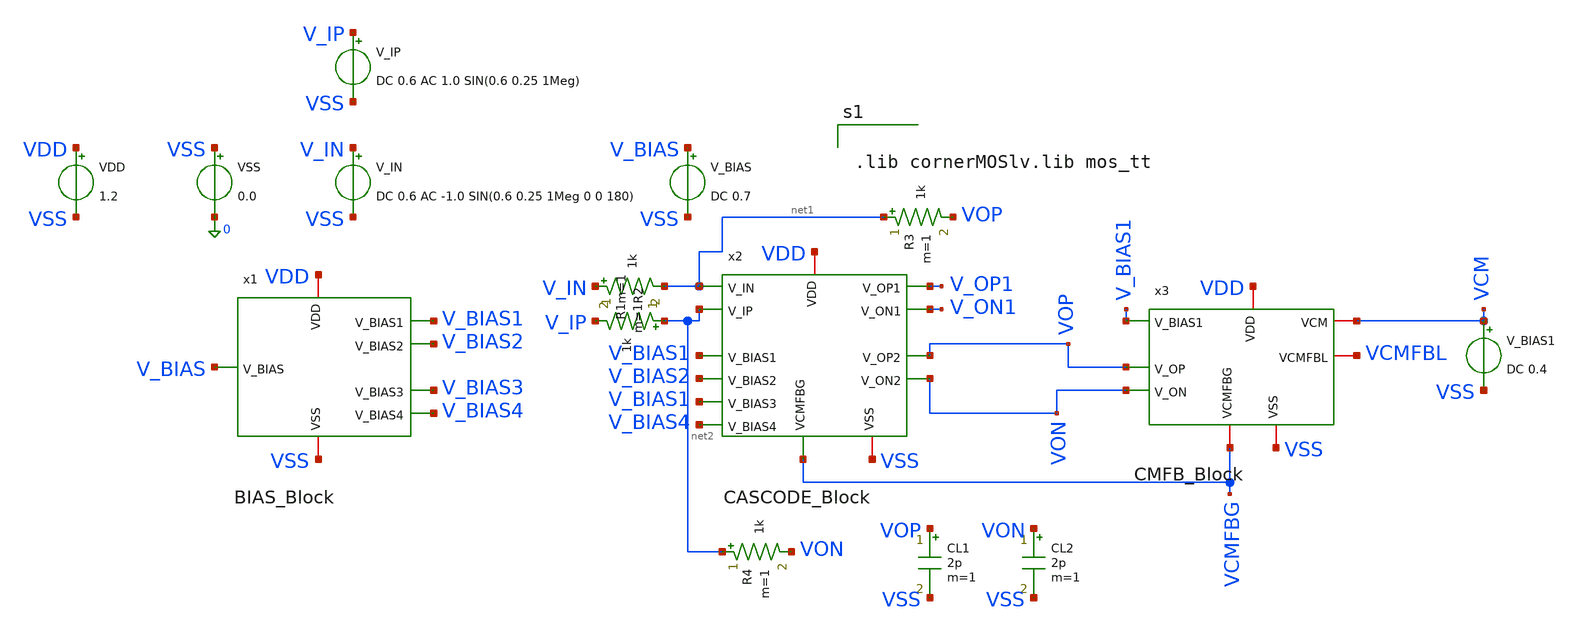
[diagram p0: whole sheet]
** sch_path: two-stage-ota-with-cmfb/Simulation/TEST_SIN.sch
**.subckt TEST_SIN
VDD VDD VSS 1.2
VSS VSS 0 0.0
V_IN V_IN VSS DC 0.6 AC -1.0 SIN(0.6 0.25 1Meg 0 0 180)
V_IP V_IP VSS DC 0.6 AC 1.0 SIN(0.6 0.25 1Meg)
V_BIAS V_BIAS VSS DC 0.7
V_BIAS1 VCM VSS DC 0.4
CL1 VOP VSS 2p m=1
x1 VSS V_BIAS4 V_BIAS2 V_BIAS3 VDD V_BIAS1 V_BIAS BIAS_Block
x2 VDD V_BIAS1 net1 net2 V_BIAS2 V_ON1 V_OP1 V_BIAS1 VON VOP VCMFBG V_BIAS4 VSS CASCODE_Block
x3 VDD V_BIAS1 VCM VOP VON VCMFBL VCMFBG VSS CMFB_Block
CL2 VON VSS 2p m=1
R1 V_IN net1 1k m=1
R2 net2 V_IP 1k m=1
R3 net1 VOP 1k m=1
R4 net2 VON 1k m=1
**** begin user architecture code


.lib cornerMOSlv.lib mos_tt




* RUN SINE RESPONSE & THD
.control
set color0=white
set color1=black

tran 1n 6u

let v_out_sine = v(vop) - v(von)
let v_in_sine  = v(v_ip) - v(v_in)

* Do bien do dinh - dinh tren cac chu ky xac lap (tu 3us den 6us)
meas tran v_max_sine max v_out_sine from=3u to=6u
meas tran v_min_sine min v_out_sine from=3u to=6u
let v_swing_pp = v_max_sine - v_min_sine

* Phan tich pho Fourier va THD
fourier 1Meg v_out_sine

echo '=========================================================================='
echo 'KET QUA LARGE-SIGNAL SINE (1 MHz):'
echo '=========================================================================='
print v_swing_pp

* Ve do thi kiem tra
plot v_in_sine v_out_sine ylabel 'Differential Voltage (V)' xlabel 'Time (s)' title 'Large-Signal 1 MHz Sinusoidal Response'
.endc


**** end user architecture code
**.ends
.end
